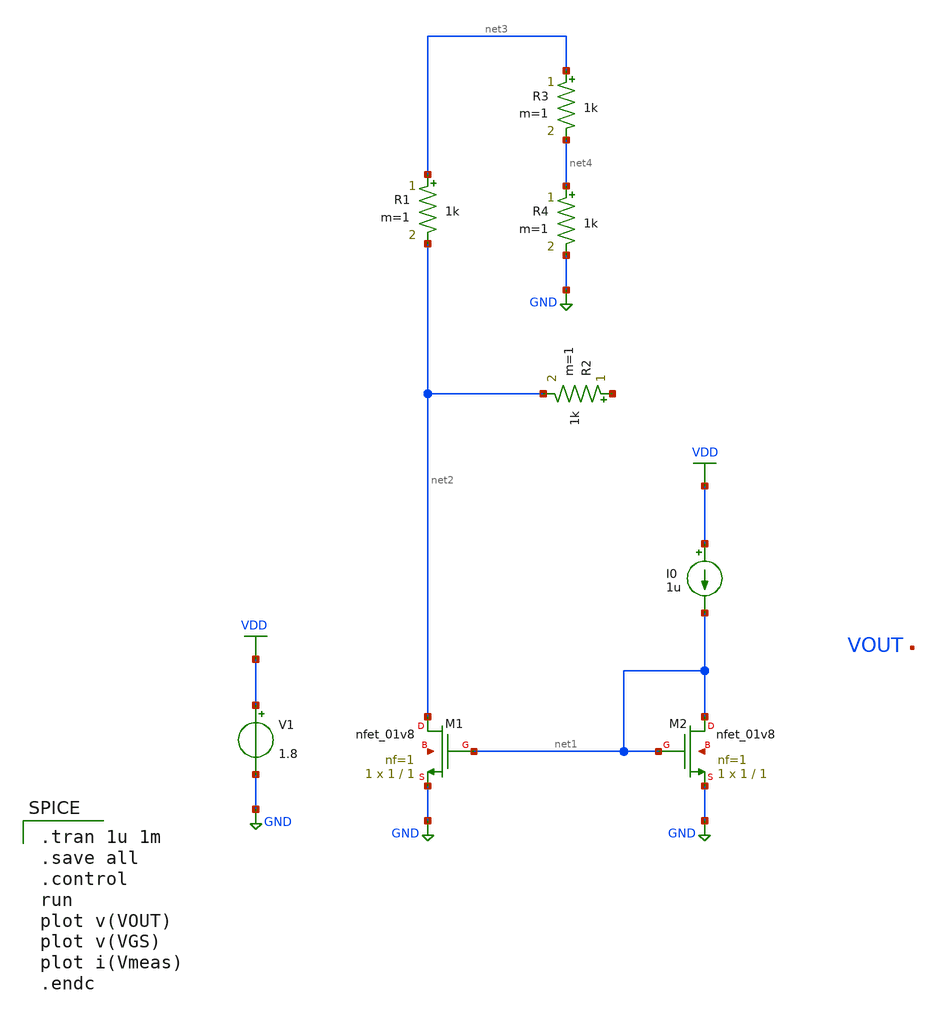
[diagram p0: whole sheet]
** sch_path: Circuits/Examples/Analog/current_comparator/curr_comp.sch
**.subckt curr_comp
V1 VDD GND 1.8
XM1 net2 net1 GND net5 sky130_fd_pr__nfet_01v8 L=1 W=1 nf=1 ad='int((nf+1)/2) * W/nf * 0.29' as='int((nf+2)/2) * W/nf * 0.29'
+ pd='2*int((nf+1)/2) * (W/nf + 0.29)' ps='2*int((nf+2)/2) * (W/nf + 0.29)' nrd='0.29 / W' nrs='0.29 / W'
+ sa=0 sb=0 sd=0 mult=1 m=1
I0 VDD net1 1u
XM2 net1 net1 GND net6 sky130_fd_pr__nfet_01v8 L=1 W=1 nf=1 ad='int((nf+1)/2) * W/nf * 0.29' as='int((nf+2)/2) * W/nf * 0.29'
+ pd='2*int((nf+1)/2) * (W/nf + 0.29)' ps='2*int((nf+2)/2) * (W/nf + 0.29)' nrd='0.29 / W' nrs='0.29 / W'
+ sa=0 sb=0 sd=0 mult=1 m=1
R1 net3 net2 1k m=1
R2 net7 net2 1k m=1
R3 net3 net4 1k m=1
R4 net4 GND 1k m=1
**** begin user architecture code
 ** manual skywater pdks install (with patches applied)
* .lib $::SKYWATER_MODELS/models/sky130.lib.spice tt

** opencircuitdesign pdks install
.lib $::SKYWATER_MODELS/sky130.lib.spice tt

.param mc_mm_switch=0
.param mc_pr_switch=0


.tran 1u 1m
.save all
.control
run
plot v(VOUT)
plot v(VGS)
plot i(Vmeas)
.endc


**** end user architecture code
**.ends
.GLOBAL GND
.GLOBAL VDD
.end
